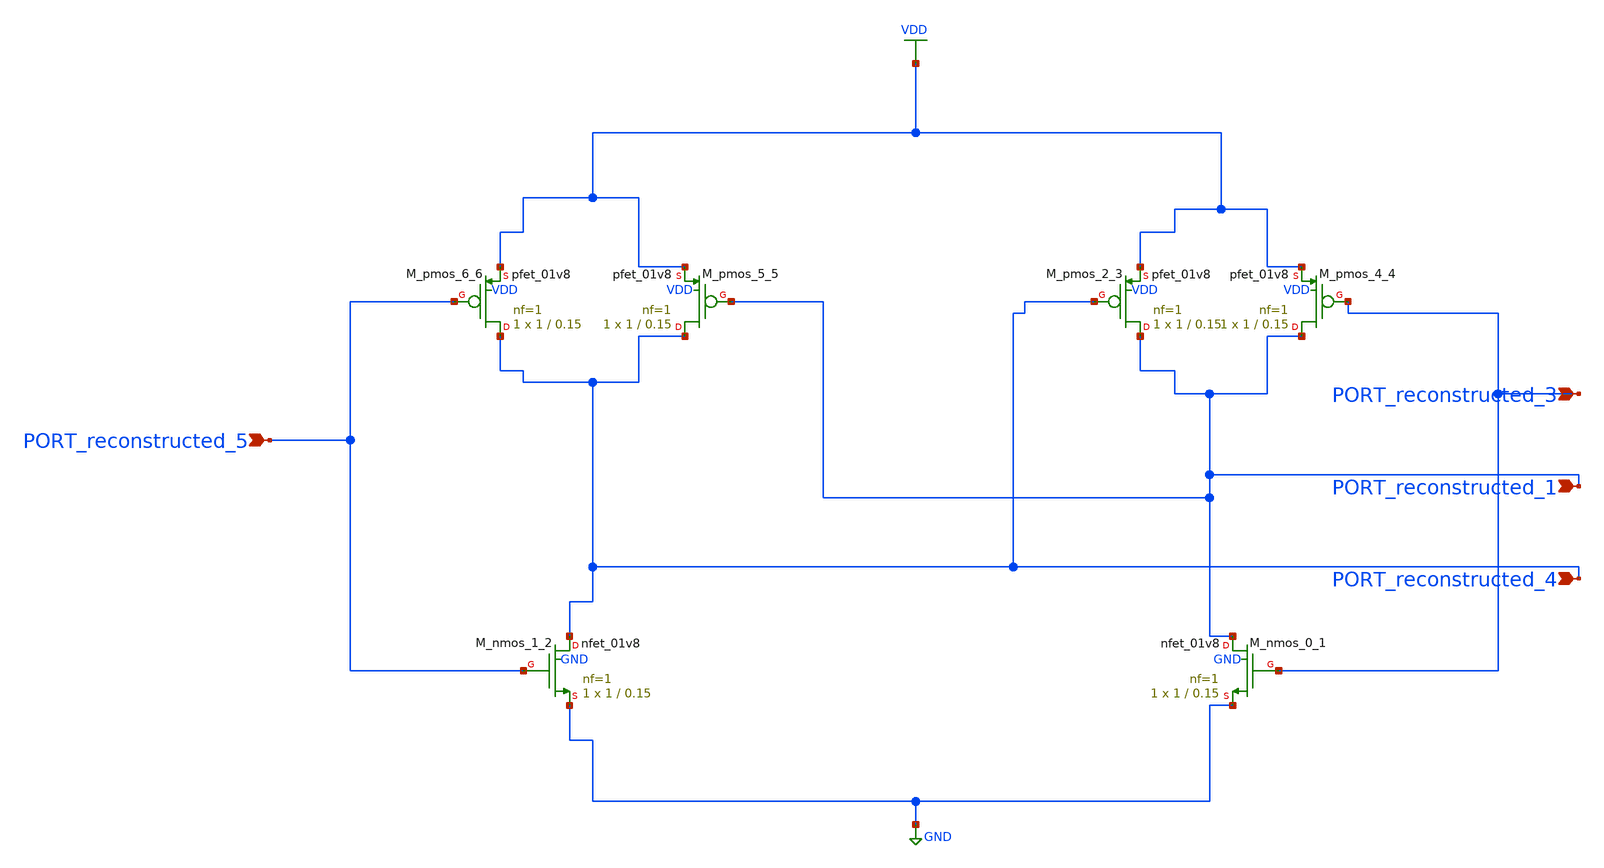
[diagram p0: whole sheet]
** sch_path: schematics/SchemGen/10_1109_ACCESS_2023_3331308_07_004.sch
**.subckt 10_1109_ACCESS_2023_3331308_07_004 PORT_reconstructed_4 PORT_reconstructed_5
*+ PORT_reconstructed_3 PORT_reconstructed_1
*.ipin PORT_reconstructed_4
*.ipin PORT_reconstructed_5
*.ipin PORT_reconstructed_3
*.ipin PORT_reconstructed_1
XM_nmos_0_1 PORT_reconstructed_1 PORT_reconstructed_3 GND GND sky130_fd_pr__nfet_01v8 L=0.15 W=1 nf=1
+ ad='int((1 + 1)/2) * 1 / 1 * 0.29' as='int((1 + 2)/2) * 1 / 1 * 0.29' pd='2*int((1 + 1)/2) * (1 / 1 + 0.29)'
+ ps='2*int((1 + 2)/2) * (1 / 1 + 0.29)' nrd='0.29 / 1 ' nrs='0.29 / 1 ' sa=0 sb=0 sd=0 mult=1 m=1
XM_nmos_1_2 PORT_reconstructed_4 PORT_reconstructed_5 GND GND sky130_fd_pr__nfet_01v8 L=0.15 W=1 nf=1
+ ad='int((1 + 1)/2) * 1 / 1 * 0.29' as='int((1 + 2)/2) * 1 / 1 * 0.29' pd='2*int((1 + 1)/2) * (1 / 1 + 0.29)'
+ ps='2*int((1 + 2)/2) * (1 / 1 + 0.29)' nrd='0.29 / 1 ' nrs='0.29 / 1 ' sa=0 sb=0 sd=0 mult=1 m=1
XM_pmos_2_3 PORT_reconstructed_1 PORT_reconstructed_4 VDD VDD sky130_fd_pr__pfet_01v8 L=0.15 W=1 nf=1
+ ad='int((1 + 1)/2) * 1 / 1 * 0.29' as='int((1 + 2)/2) * 1 / 1 * 0.29' pd='2*int((1 + 1)/2) * (1 / 1 + 0.29)'
+ ps='2*int((1 + 2)/2) * (1 / 1 + 0.29)' nrd='0.29 / 1 ' nrs='0.29 / 1 ' sa=0 sb=0 sd=0 mult=1 m=1
XM_pmos_4_4 PORT_reconstructed_1 PORT_reconstructed_3 VDD VDD sky130_fd_pr__pfet_01v8 L=0.15 W=1 nf=1
+ ad='int((1 + 1)/2) * 1 / 1 * 0.29' as='int((1 + 2)/2) * 1 / 1 * 0.29' pd='2*int((1 + 1)/2) * (1 / 1 + 0.29)'
+ ps='2*int((1 + 2)/2) * (1 / 1 + 0.29)' nrd='0.29 / 1 ' nrs='0.29 / 1 ' sa=0 sb=0 sd=0 mult=1 m=1
XM_pmos_5_5 PORT_reconstructed_4 PORT_reconstructed_1 VDD VDD sky130_fd_pr__pfet_01v8 L=0.15 W=1 nf=1
+ ad='int((1 + 1)/2) * 1 / 1 * 0.29' as='int((1 + 2)/2) * 1 / 1 * 0.29' pd='2*int((1 + 1)/2) * (1 / 1 + 0.29)'
+ ps='2*int((1 + 2)/2) * (1 / 1 + 0.29)' nrd='0.29 / 1 ' nrs='0.29 / 1 ' sa=0 sb=0 sd=0 mult=1 m=1
XM_pmos_6_6 PORT_reconstructed_4 PORT_reconstructed_5 VDD VDD sky130_fd_pr__pfet_01v8 L=0.15 W=1 nf=1
+ ad='int((1 + 1)/2) * 1 / 1 * 0.29' as='int((1 + 2)/2) * 1 / 1 * 0.29' pd='2*int((1 + 1)/2) * (1 / 1 + 0.29)'
+ ps='2*int((1 + 2)/2) * (1 / 1 + 0.29)' nrd='0.29 / 1 ' nrs='0.29 / 1 ' sa=0 sb=0 sd=0 mult=1 m=1
**.ends
.GLOBAL GND
.GLOBAL VDD
.end
